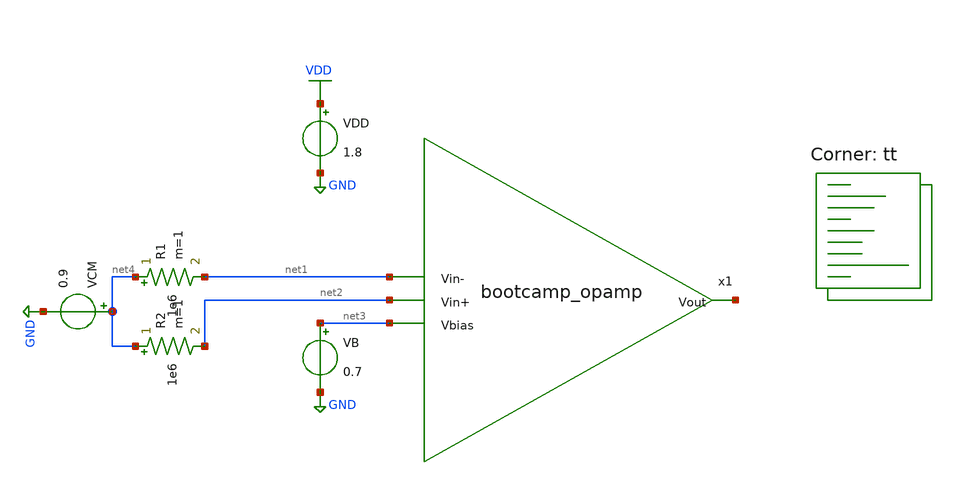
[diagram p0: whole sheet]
** sch_path: analog/schematics/tb_cmrr.sch
**.subckt tb_cmrr
x1 net5 net1 net2 net3 bootcamp_opamp
VDD VDD GND 1.8
VCM net4 GND 0.9
VB net3 GND 0.7
R1 net4 net1 1e6 m=1
R2 net4 net2 1e6 m=1
**** begin user architecture code
.lib $::SKYWATER_MODELS/sky130.lib.spice tt
**** end user architecture code
**.ends
.GLOBAL GND
.GLOBAL VDD
.end
